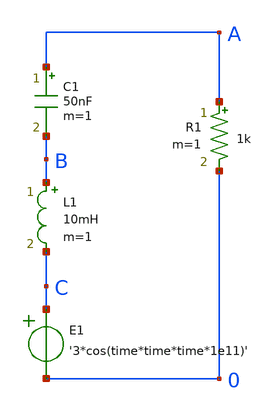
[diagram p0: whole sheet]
** sch_path: rlc.sch.sch
**.subckt rlc.sch
C1 A B 50nF m=1
R1 A 0 1k m=1
L1 B C 10mH m=1
E1 C 0 VOL=' '3*cos(time*time*time*1e11)' '
**** begin user architecture code


.tran 10n 2000u uic
.save all


**** end user architecture code
**.ends
.end
